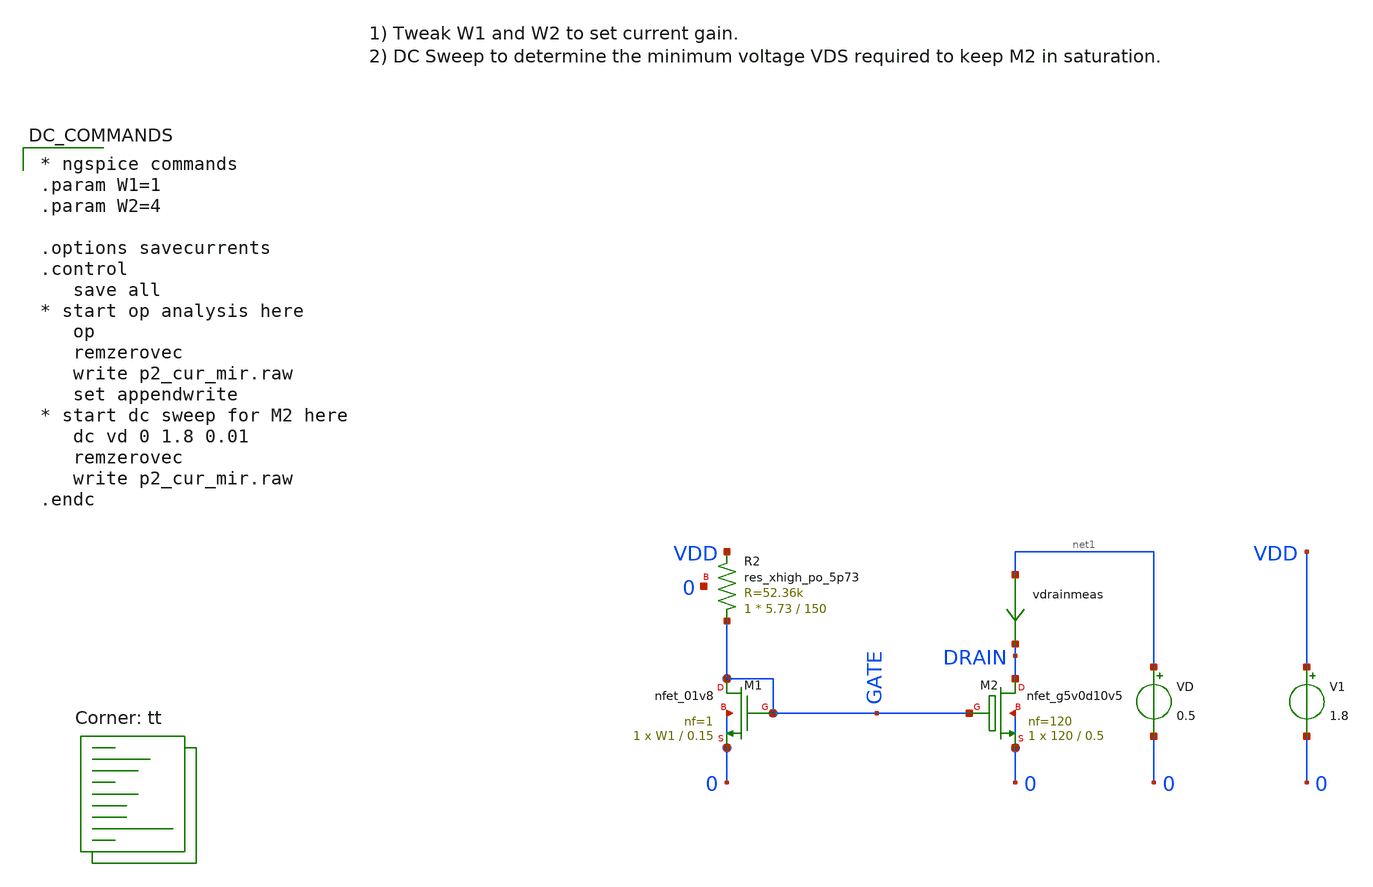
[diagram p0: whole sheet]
** sch_path: xschem/p2_cur_mir.sch
**.subckt p2_cur_mir
XM1 GATE GATE 0 0 sky130_fd_pr__nfet_01v8 L=0.15 W=W1 nf=1 ad='int((nf+1)/2) * W/nf * 0.29' as='int((nf+2)/2) * W/nf * 0.29'
+ pd='2*int((nf+1)/2) * (W/nf + 0.29)' ps='2*int((nf+2)/2) * (W/nf + 0.29)' nrd='0.29 / W' nrs='0.29 / W'
+ sa=0 sb=0 sd=0 mult=1 m=1
VD net1 0 0.5
vdrainmeas net1 DRAIN 0
.save i(vdrainmeas)
V1 VDD 0 1.8
XR2 GATE VDD 0 sky130_fd_pr__res_xhigh_po_5p73 L=150 mult=1 m=1
XM2 DRAIN GATE 0 0 sky130_fd_pr__nfet_g5v0d10v5 L=0.5 W=120 nf=120 ad='int((nf+1)/2) * W/nf * 0.29' as='int((nf+2)/2) * W/nf * 0.29'
+ pd='2*int((nf+1)/2) * (W/nf + 0.29)' ps='2*int((nf+2)/2) * (W/nf + 0.29)' nrd='0.29 / W' nrs='0.29 / W'
+ sa=0 sb=0 sd=0 mult=1 m=1
**** begin user architecture code
.lib $::SKYWATER_MODELS/sky130.lib.spice tt

* ngspice commands
.param W1=1
.param W2=4

.options savecurrents
.control
   save all
* start op analysis here
   op
   remzerovec
   write p2_cur_mir.raw
   set appendwrite
* start dc sweep for M2 here
   dc vd 0 1.8 0.01
   remzerovec
   write p2_cur_mir.raw
.endc


**** end user architecture code
**.ends
.end
